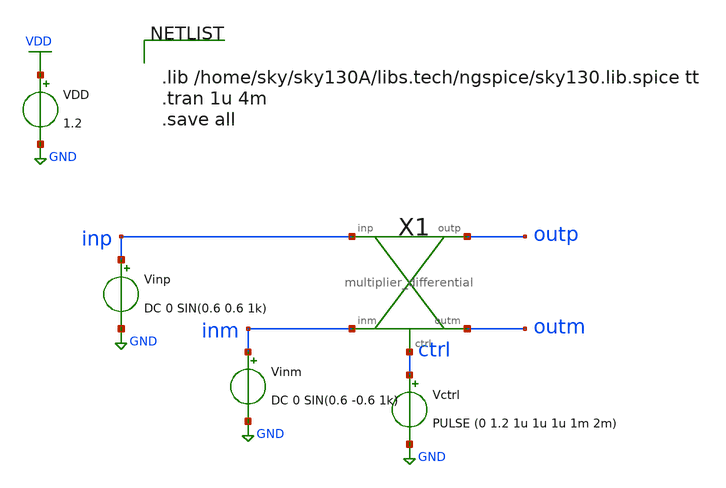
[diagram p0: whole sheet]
** sch_path: xschem/mux/multiplier_differential_tb.sch
**.subckt multiplier_differential_tb
Vinp inp GND DC 0 SIN(0.6 0.6 1k)
VDD VDD GND 1.2
Vctrl ctrl GND PULSE (0 1.2 1u 1u 1u 1m 2m)
Vinm inm GND DC 0 SIN(0.6 -0.6 1k)
X1 inp outp inm ctrl outm multiplier_differential
**** begin user architecture code


.lib /home/sky/sky130A/libs.tech/ngspice/sky130.lib.spice tt
.tran 1u 4m
.save all


**** end user architecture code
**.ends

* expanding   symbol:  mux/multiplier_differential.sym # of pins=5
** sym_path: xschem/mux/multiplier_differential.sym
** sch_path: xschem/mux/multiplier_differential.sch
.subckt multiplier_differential inp outp inm ctrl outm
*.ipin inp
*.ipin inm
*.opin outp
*.opin outm
*.ipin ctrl
X1 inp outp inm ctrl mux2-1
X2 inm outm inp ctrl mux2-1
.ends


* expanding   symbol:  mux/mux2-1.sym # of pins=4
** sym_path: xschem/mux/mux2-1.sym
** sch_path: xschem/mux/mux2-1.sch
.subckt mux2-1 in1 out in2 ctrl
*.ipin in1
*.ipin ctrl
*.ipin in2
*.iopin out
X1 in1 out net1 ctrl transmission_gate Wpmos=3 Lpmos=0.18 Wnmos=1 Lnmos=0.18
X2 in2 out ctrl net1 transmission_gate Wpmos=3 Lpmos=0.18 Wnmos=1 Lnmos=0.18
X4 ctrl net1 inv Wpmos=3 Lpmos=0.18 Wnmos=1 Lnmos=0.18
.ends


* expanding   symbol:  transmission_gate/transmission_gate.sym # of pins=4
** sym_path: xschem/transmission_gate/transmission_gate.sym
** sch_path: xschem/transmission_gate/transmission_gate.sch
.subckt transmission_gate in out ctrl_ ctrl  Wpmos=1 Lpmos=0.18 Wnmos=1 Lnmos=0.18
*.iopin in
*.iopin out
*.ipin ctrl_
*.ipin ctrl
XM1 in ctrl out GND sky130_fd_pr__nfet_01v8 L=Lnmos W=Wnmos nf=1 ad='int((nf+1)/2) * W/nf * 0.29' as='int((nf+2)/2) * W/nf * 0.29'
+ pd='2*int((nf+1)/2) * (W/nf + 0.29)' ps='2*int((nf+2)/2) * (W/nf + 0.29)' nrd='0.29 / W' nrs='0.29 / W'
+ sa=0 sb=0 sd=0 mult=1 m=1
XM2 out ctrl_ in VDD sky130_fd_pr__pfet_01v8 L=Lpmos W=Wpmos nf=1 ad='int((nf+1)/2) * W/nf * 0.29' as='int((nf+2)/2) * W/nf * 0.29'
+ pd='2*int((nf+1)/2) * (W/nf + 0.29)' ps='2*int((nf+2)/2) * (W/nf + 0.29)' nrd='0.29 / W' nrs='0.29 / W'
+ sa=0 sb=0 sd=0 mult=1 m=1
.ends


* expanding   symbol:  inv/inv.sym # of pins=2
** sym_path: xschem/inv/inv.sym
** sch_path: xschem/inv/inv.sch
.subckt inv in out  Wpmos=3 Lpmos=0.18 Wnmos=1 Lnmos=0.18
*.ipin in
*.iopin out
XM1 out in GND GND sky130_fd_pr__nfet_01v8 L=Lnmos W=Wnmos nf=1 ad='int((nf+1)/2) * W/nf * 0.29' as='int((nf+2)/2) * W/nf * 0.29'
+ pd='2*int((nf+1)/2) * (W/nf + 0.29)' ps='2*int((nf+2)/2) * (W/nf + 0.29)' nrd='0.29 / W' nrs='0.29 / W'
+ sa=0 sb=0 sd=0 mult=1 m=1
XM2 out in VDD VDD sky130_fd_pr__pfet_01v8 L=Lpmos W=Wpmos nf=1 ad='int((nf+1)/2) * W/nf * 0.29' as='int((nf+2)/2) * W/nf * 0.29'
+ pd='2*int((nf+1)/2) * (W/nf + 0.29)' ps='2*int((nf+2)/2) * (W/nf + 0.29)' nrd='0.29 / W' nrs='0.29 / W'
+ sa=0 sb=0 sd=0 mult=1 m=1
.ends

.GLOBAL VDD
.GLOBAL GND
.end
